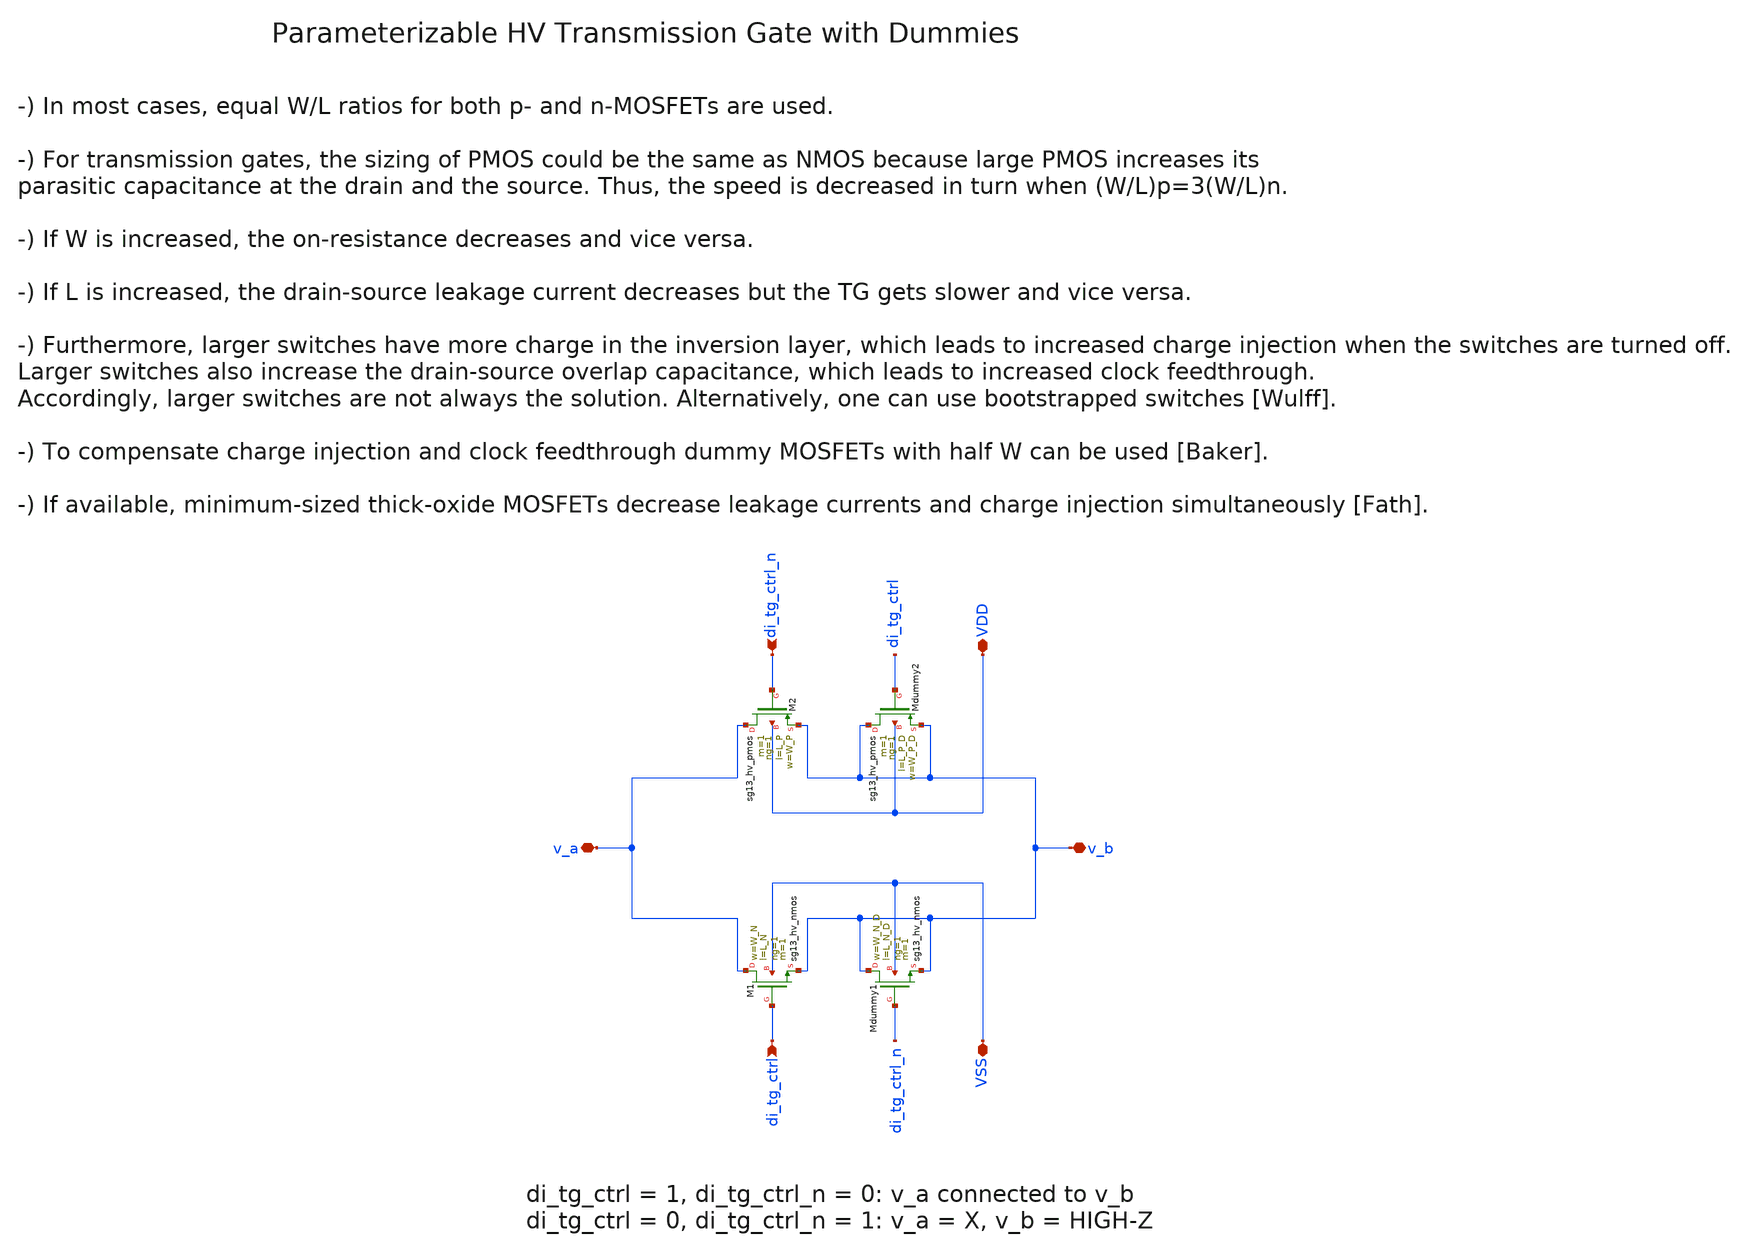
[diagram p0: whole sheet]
** sch_path: SG13G2_ATBS-ADC-main/xschem/transmission_gate/transmission_gate_hv_w_dummy.sch
**.subckt transmission_gate_hv_w_dummy v_a v_b VDD VSS di_tg_ctrl di_tg_ctrl_n
*.iopin v_a
*.iopin v_b
*.iopin VDD
*.iopin VSS
*.ipin di_tg_ctrl
*.ipin di_tg_ctrl_n
XM1 v_a di_tg_ctrl v_b VSS sg13_hv_nmos w=W_N l=L_N ng=1 m=1 mm_ok=1
XM2 v_a di_tg_ctrl_n v_b VDD sg13_hv_pmos w=W_P l=L_P ng=1 m=1 mm_ok=1
XMdummy1 v_b di_tg_ctrl_n v_b VSS sg13_hv_nmos w=W_N_D l=L_N_D ng=1 m=1 mm_ok=1
XMdummy2 v_b di_tg_ctrl v_b VDD sg13_hv_pmos w=W_P_D l=L_P_D ng=1 m=1 mm_ok=1
**.ends
.end
